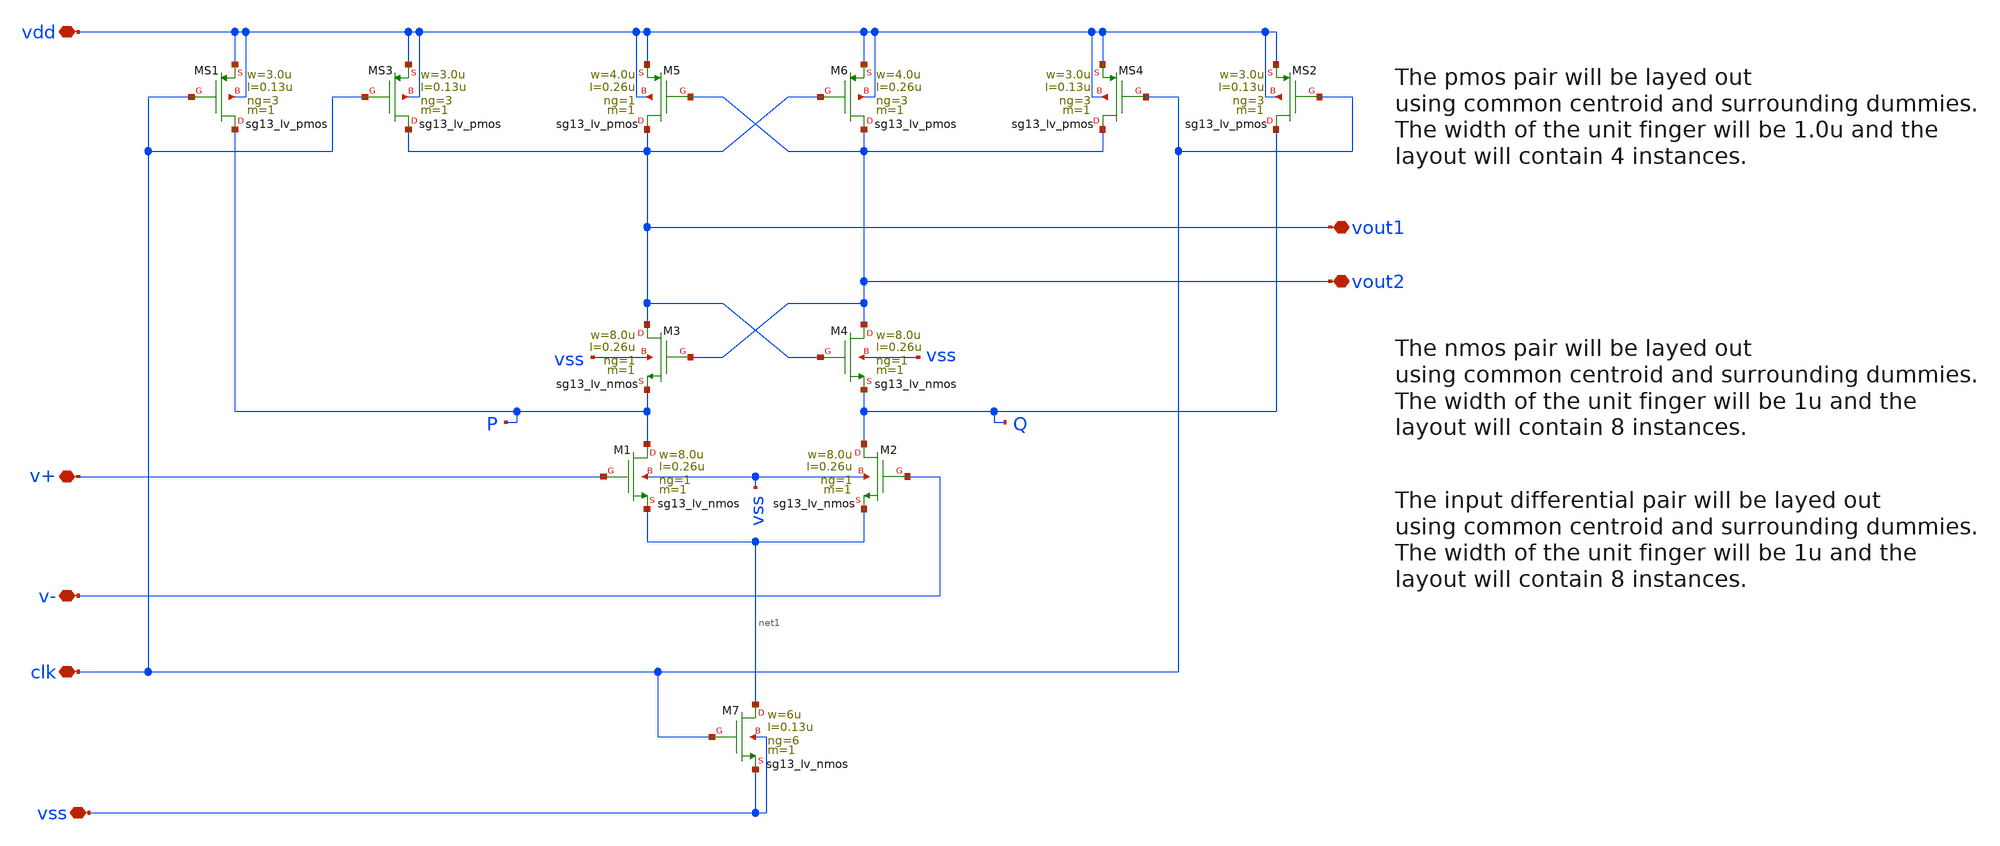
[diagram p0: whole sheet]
** sch_path: CMP7345-main/schematic/xschem/CMP7345-basic.sch
**.subckt CMP7345-basic v- v+ vss vdd clk vout2 vout1
*.iopin v-
*.iopin v+
*.iopin vss
*.iopin vdd
*.iopin clk
*.iopin vout2
*.iopin vout1
XM2 Q v- net1 vss sg13_lv_nmos w=8.0u l=0.26u ng=1 m=1 mm_ok=1
XM1 P v+ net1 vss sg13_lv_nmos w=8.0u l=0.26u ng=1 m=1 mm_ok=1
XM5 vout1 vout2 vdd vdd sg13_lv_pmos w=4.0u l=0.26u ng=1 m=1 mm_ok=0
XM3 vout1 vout2 P vss sg13_lv_nmos w=8.0u l=0.26u ng=1 m=1 mm_ok=1
XM7 net1 clk vss vss sg13_lv_nmos w=6u l=0.13u ng=6 m=1 mm_ok=0
XM4 vout2 vout1 Q vss sg13_lv_nmos w=8.0u l=0.26u ng=1 m=1 mm_ok=1
XM6 vout2 vout1 vdd vdd sg13_lv_pmos w=4.0u l=0.26u ng=3 m=1 mm_ok=0
XMS4 vout2 clk vdd vdd sg13_lv_pmos w=3.0u l=0.13u ng=3 m=1 mm_ok=0
XMS1 P clk vdd vdd sg13_lv_pmos w=3.0u l=0.13u ng=3 m=1 mm_ok=0
XMS2 Q clk vdd vdd sg13_lv_pmos w=3.0u l=0.13u ng=3 m=1 mm_ok=0
XMS3 vout1 clk vdd vdd sg13_lv_pmos w=3.0u l=0.13u ng=3 m=1 mm_ok=0
**.ends
.end
